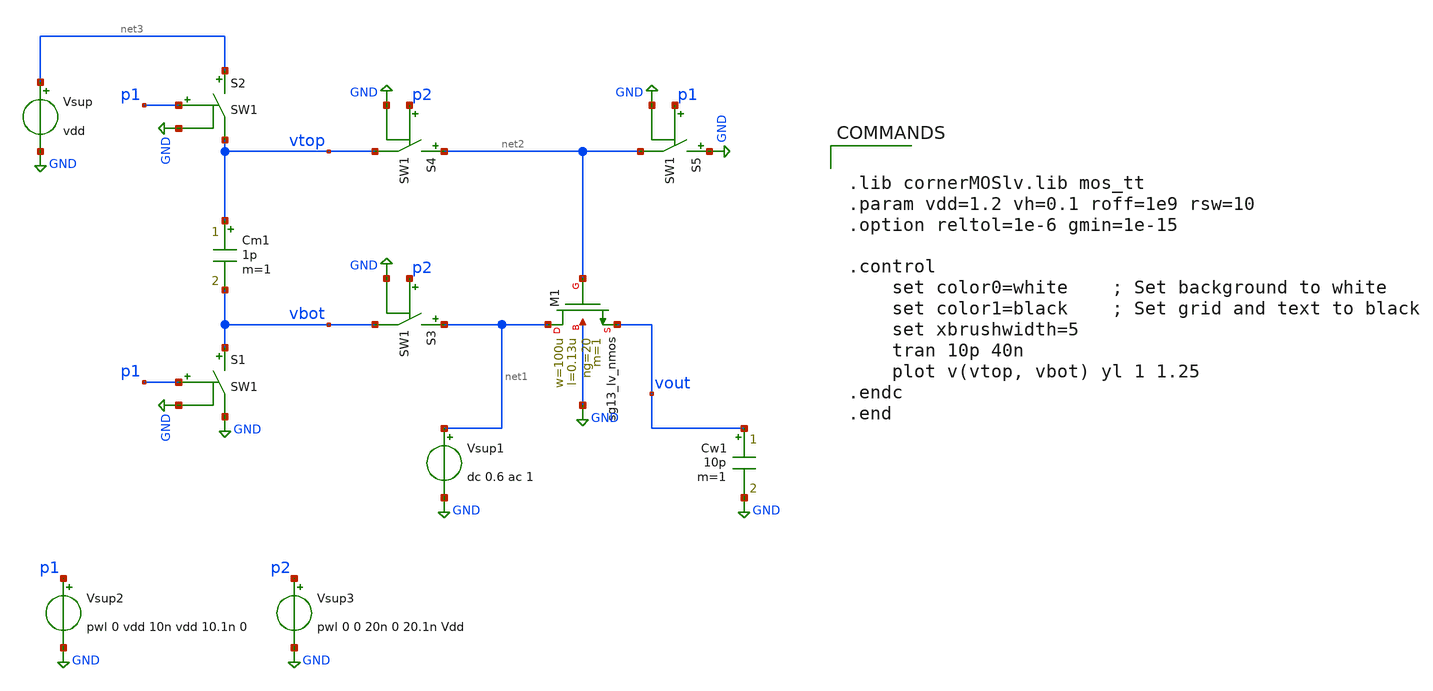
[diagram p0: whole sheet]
** sch_path: xschem/tb_clarge.sch
**.subckt tb_clarge
Vsup net3 GND vdd
Cw1 vout GND 10p m=1
Vsup1 net1 GND dc 0.6 ac 1
Cm1 vtop vbot 1p m=1
XM1 net1 net2 vout GND sg13_lv_nmos w=100u l=0.13u ng=20 m=1 mm_ok=1
Vsup2 p1 GND pwl 0 vdd 10n vdd 10.1n 0
Vsup3 p2 GND pwl 0 0 20n 0 20.1n Vdd
S1 vbot GND p1 GND SW1
S2 net3 vtop p1 GND SW1
S3 net1 vbot p2 GND SW1
S4 net2 vtop p2 GND SW1
S5 GND net2 p1 GND SW1
**** begin user architecture code


.lib cornerMOSlv.lib mos_tt
.param vdd=1.2 vh=0.1 roff=1e9 rsw=10
.option reltol=1e-6 gmin=1e-15

.control
    set color0=white    ; Set background to white
    set color1=black    ; Set grid and text to black
    set xbrushwidth=5
    tran 10p 40n
    plot v(vtop, vbot) yl 1 1.25
.endc
.end


**** end user architecture code
**.ends
.GLOBAL GND
**** begin user architecture code
.MODEL SW1 SW   VT=0.9 VH=0  RON=10 ROFF=10G
**** end user architecture code
.end
